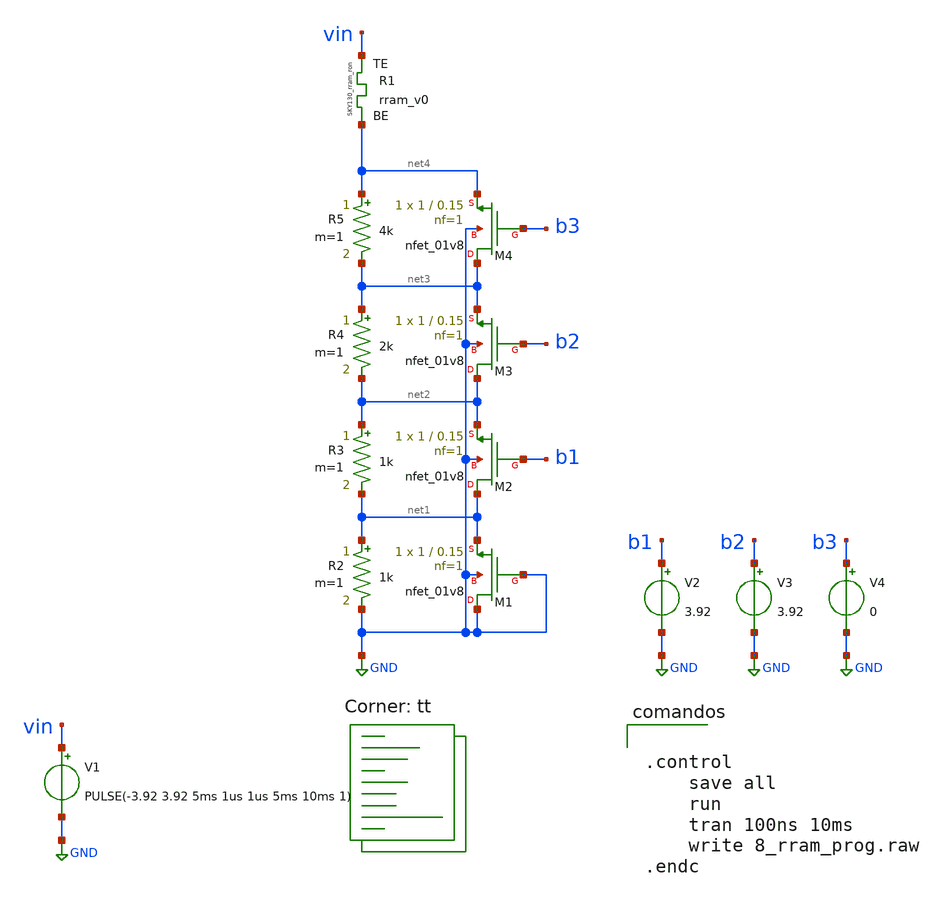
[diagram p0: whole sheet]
** sch_path: rram_programming/4_rram_prog.sch
**.subckt 4_rram_prog
V1 vin GND PULSE(-3.92 3.92 5ms 1us 1us 5ms 10ms 1)
XR1 vin net4 rram_v0
R2 net1 GND 1k m=1
R3 net2 net1 1k m=1
R4 net3 net2 2k m=1
XM4 net3 b3 net4 GND sky130_fd_pr__nfet_01v8 L=0.15 W=1 nf=1 ad='int((nf+1)/2) * W/nf * 0.29' as='int((nf+2)/2) * W/nf * 0.29'
+ pd='2*int((nf+1)/2) * (W/nf + 0.29)' ps='2*int((nf+2)/2) * (W/nf + 0.29)' nrd='0.29 / W' nrs='0.29 / W'
+ sa=0 sb=0 sd=0 mult=1 m=1
R5 net4 net3 4k m=1
V2 b1 GND 3.92
V3 b2 GND 3.92
V4 b3 GND 0
XM1 GND GND net1 GND sky130_fd_pr__nfet_01v8 L=0.15 W=1 nf=1 ad='int((nf+1)/2) * W/nf * 0.29' as='int((nf+2)/2) * W/nf * 0.29'
+ pd='2*int((nf+1)/2) * (W/nf + 0.29)' ps='2*int((nf+2)/2) * (W/nf + 0.29)' nrd='0.29 / W' nrs='0.29 / W'
+ sa=0 sb=0 sd=0 mult=1 m=1
XM2 net1 b1 net2 GND sky130_fd_pr__nfet_01v8 L=0.15 W=1 nf=1 ad='int((nf+1)/2) * W/nf * 0.29' as='int((nf+2)/2) * W/nf * 0.29'
+ pd='2*int((nf+1)/2) * (W/nf + 0.29)' ps='2*int((nf+2)/2) * (W/nf + 0.29)' nrd='0.29 / W' nrs='0.29 / W'
+ sa=0 sb=0 sd=0 mult=1 m=1
XM3 net2 b2 net3 GND sky130_fd_pr__nfet_01v8 L=0.15 W=1 nf=1 ad='int((nf+1)/2) * W/nf * 0.29' as='int((nf+2)/2) * W/nf * 0.29'
+ pd='2*int((nf+1)/2) * (W/nf + 0.29)' ps='2*int((nf+2)/2) * (W/nf + 0.29)' nrd='0.29 / W' nrs='0.29 / W'
+ sa=0 sb=0 sd=0 mult=1 m=1
**** begin user architecture code
.lib $::SKYWATER_MODELS/sky130.lib.spice tt

** opencircuitdesign pdks install
.inc $::SKYWATER_MODELS/rram_v0.spice



.control
	save all
	run
	tran 100ns 10ms
	write 8_rram_prog.raw
.endc



**** end user architecture code
**.ends
.GLOBAL GND
.end
